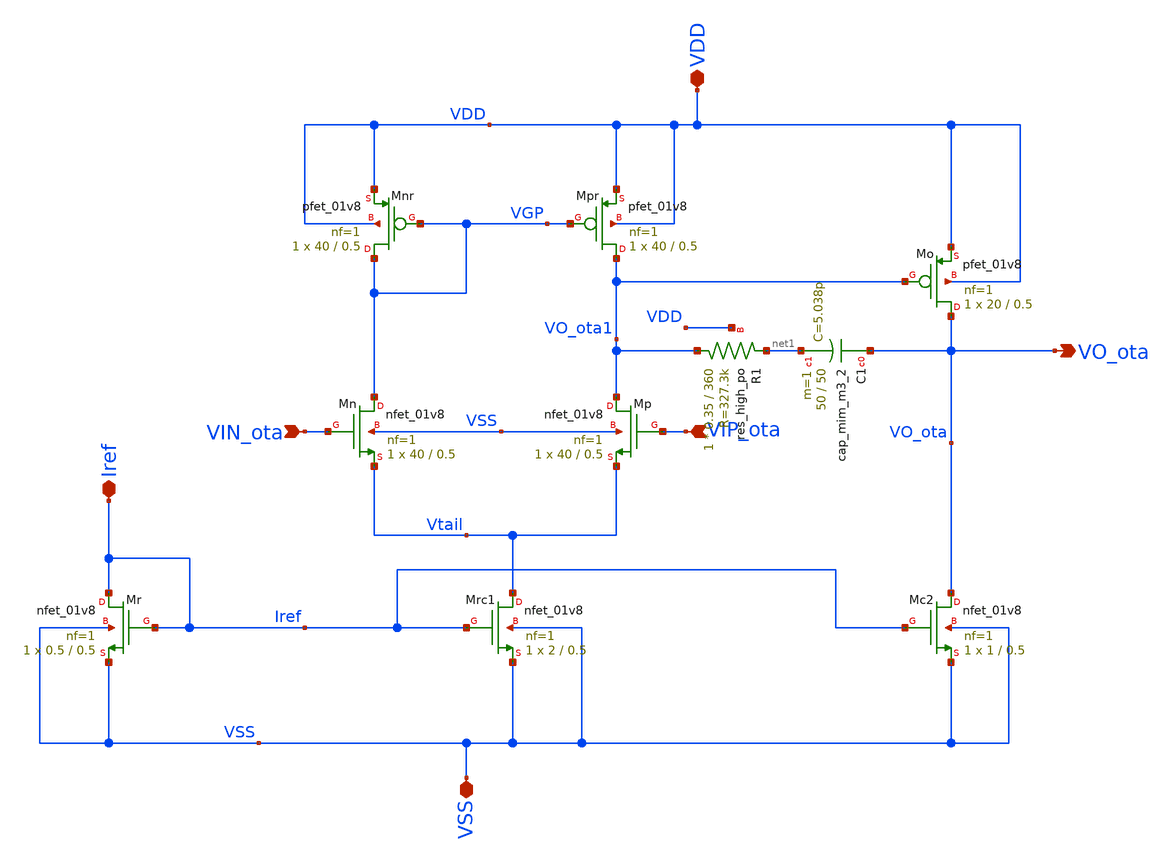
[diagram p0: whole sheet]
** sch_path: xschem/OTA.sch
**.subckt OTA VIN_ota VO_ota Iref VSS VDD VIP_ota
*.ipin VIN_ota
*.opin VO_ota
*.iopin Iref
*.iopin VSS
*.iopin VDD
*.ipin VIP_ota
XMr Iref Iref VSS VSS sky130_fd_pr__nfet_01v8 L=0.5 W=0.5 nf=1 ad='int((1 + 1)/2) * 0.5 / 1 * 0.29' as='int((1 + 2)/2) * 0.5 / 1 * 0.29'
+ pd='2*int((1 + 1)/2) * (0.5 / 1 + 0.29)' ps='2*int((1 + 2)/2) * (0.5 / 1 + 0.29)' nrd='0.29 / 0.5 ' nrs='0.29 / 0.5 '
+ sa=0 sb=0 sd=0 mult=1 m=1
XMo VO_ota VO_ota1 VDD VDD sky130_fd_pr__pfet_01v8 L=0.5 W=20 nf=1 ad='int((1 + 1)/2) * 20 / 1 * 0.29'
+ as='int((1 + 2)/2) * 20 / 1 * 0.29' pd='2*int((1 + 1)/2) * (20 / 1 + 0.29)' ps='2*int((1 + 2)/2) * (20 / 1 + 0.29)'
+ nrd='0.29 / 20 ' nrs='0.29 / 20 ' sa=0 sb=0 sd=0 mult=1 m=1
XMrc1 Vtail Iref VSS VSS sky130_fd_pr__nfet_01v8 L=0.5 W=2 nf=1 ad='int((1 + 1)/2) * 2 / 1 * 0.29' as='int((1 + 2)/2) * 2 / 1 * 0.29'
+ pd='2*int((1 + 1)/2) * (2 / 1 + 0.29)' ps='2*int((1 + 2)/2) * (2 / 1 + 0.29)' nrd='0.29 / 2 ' nrs='0.29 / 2 '
+ sa=0 sb=0 sd=0 mult=1 m=1
XMc2 VO_ota Iref VSS VSS sky130_fd_pr__nfet_01v8 L=0.5 W=1 nf=1 ad='int((1 + 1)/2) * 1 / 1 * 0.29' as='int((1 + 2)/2) * 1 / 1 * 0.29'
+ pd='2*int((1 + 1)/2) * (1 / 1 + 0.29)' ps='2*int((1 + 2)/2) * (1 / 1 + 0.29)' nrd='0.29 / 1 ' nrs='0.29 / 1 '
+ sa=0 sb=0 sd=0 mult=1 m=1
XMn VGP VIN_ota Vtail VSS sky130_fd_pr__nfet_01v8 L=0.5 W=40 nf=1 ad='int((1 + 1)/2) * 40 / 1 * 0.29'
+ as='int((1 + 2)/2) * 40 / 1 * 0.29' pd='2*int((1 + 1)/2) * (40 / 1 + 0.29)' ps='2*int((1 + 2)/2) * (40 / 1 + 0.29)'
+ nrd='0.29 / 40 ' nrs='0.29 / 40 ' sa=0 sb=0 sd=0 mult=1 m=1
XMp VO_ota1 VIP_ota Vtail VSS sky130_fd_pr__nfet_01v8 L=0.5 W=40 nf=1 ad='int((1 + 1)/2) * 40 / 1 * 0.29'
+ as='int((1 + 2)/2) * 40 / 1 * 0.29' pd='2*int((1 + 1)/2) * (40 / 1 + 0.29)' ps='2*int((1 + 2)/2) * (40 / 1 + 0.29)'
+ nrd='0.29 / 40 ' nrs='0.29 / 40 ' sa=0 sb=0 sd=0 mult=1 m=1
XMpr VO_ota1 VGP VDD VDD sky130_fd_pr__pfet_01v8 L=0.5 W=40 nf=1 ad='int((1 + 1)/2) * 40 / 1 * 0.29'
+ as='int((1 + 2)/2) * 40 / 1 * 0.29' pd='2*int((1 + 1)/2) * (40 / 1 + 0.29)' ps='2*int((1 + 2)/2) * (40 / 1 + 0.29)'
+ nrd='0.29 / 40 ' nrs='0.29 / 40 ' sa=0 sb=0 sd=0 mult=1 m=1
XMnr VGP VGP VDD VDD sky130_fd_pr__pfet_01v8 L=0.5 W=40 nf=1 ad='int((1 + 1)/2) * 40 / 1 * 0.29' as='int((1 + 2)/2) * 40 / 1 * 0.29'
+ pd='2*int((1 + 1)/2) * (40 / 1 + 0.29)' ps='2*int((1 + 2)/2) * (40 / 1 + 0.29)' nrd='0.29 / 40 ' nrs='0.29 / 40 '
+ sa=0 sb=0 sd=0 mult=1 m=1
XR1 VO_ota1 net1 VDD sky130_fd_pr__res_high_po W=0.35 L=360 mult=1 m=1
XC1 VO_ota net1 sky130_fd_pr__cap_mim_m3_2 W=50 L=50 MF=1 m=1
**.ends
.end
